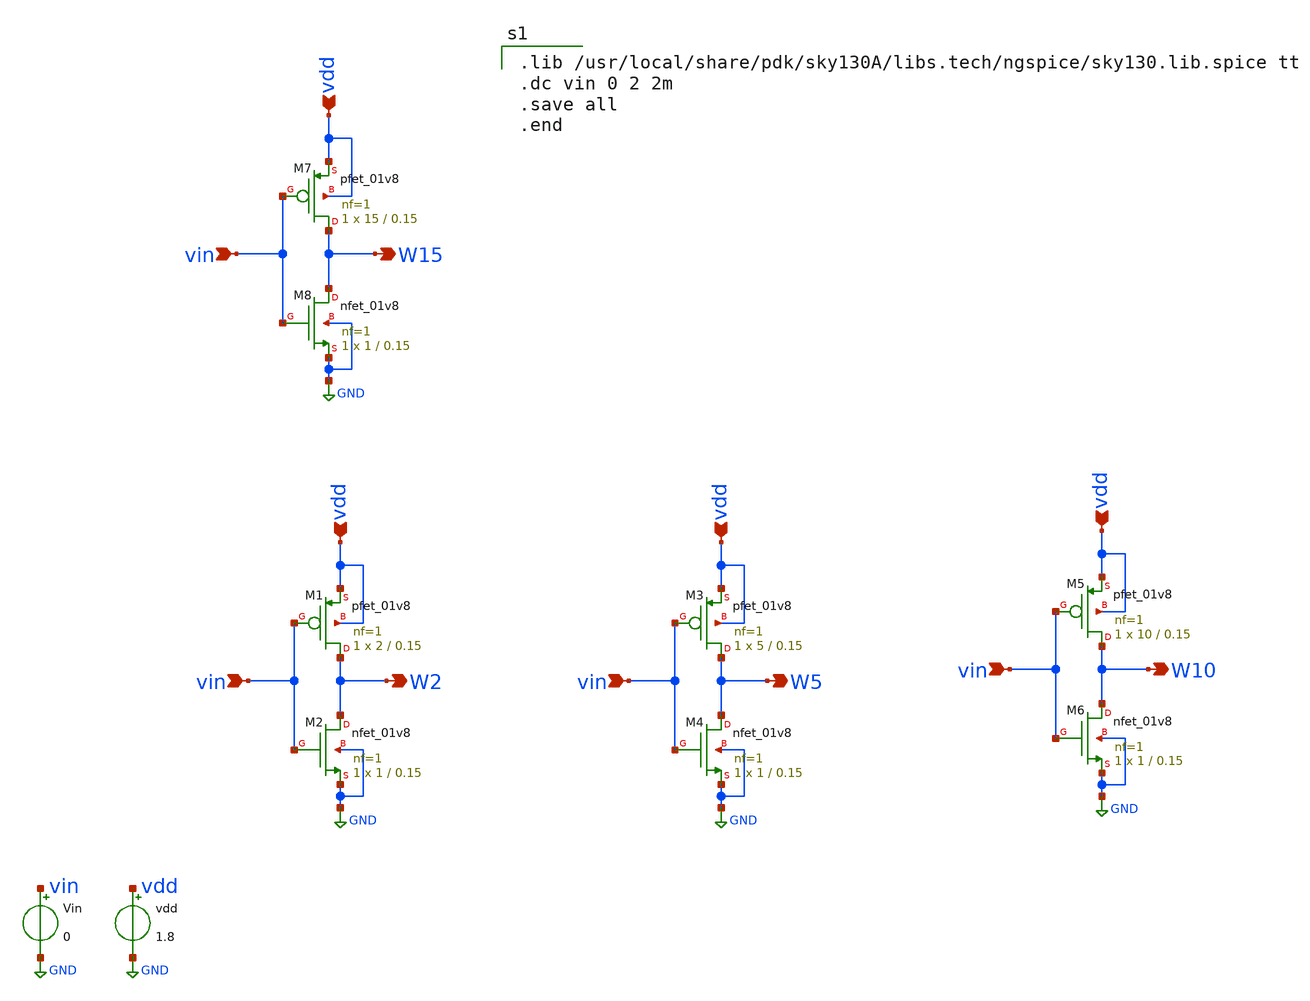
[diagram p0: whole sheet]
** sch_path: Inverter_vtc_testbench_sky130pdk.sch
**.subckt Inverter_vtc_testbench_sky130pdk vin vdd W2 vin vdd W5 vin vdd W10 vin vdd W15
*.ipin vin
*.ipin vdd
*.opin W2
*.ipin vin
*.ipin vdd
*.opin W5
*.ipin vin
*.ipin vdd
*.opin W10
*.ipin vin
*.ipin vdd
*.opin W15
XM1 W2 vin vdd vdd sky130_fd_pr__pfet_01v8 L=0.15 W=2 nf=1 ad='int((nf+1)/2) * W/nf * 0.29' as='int((nf+2)/2) * W/nf * 0.29'
+ pd='2*int((nf+1)/2) * (W/nf + 0.29)' ps='2*int((nf+2)/2) * (W/nf + 0.29)' nrd='0.29 / W' nrs='0.29 / W'
+ sa=0 sb=0 sd=0 mult=1 m=1
XM2 W2 vin GND GND sky130_fd_pr__nfet_01v8 L=0.15 W=1 nf=1 ad='int((nf+1)/2) * W/nf * 0.29' as='int((nf+2)/2) * W/nf * 0.29'
+ pd='2*int((nf+1)/2) * (W/nf + 0.29)' ps='2*int((nf+2)/2) * (W/nf + 0.29)' nrd='0.29 / W' nrs='0.29 / W'
+ sa=0 sb=0 sd=0 mult=1 m=1
XM3 W5 vin vdd vdd sky130_fd_pr__pfet_01v8 L=0.15 W=5 nf=1 ad='int((nf+1)/2) * W/nf * 0.29' as='int((nf+2)/2) * W/nf * 0.29'
+ pd='2*int((nf+1)/2) * (W/nf + 0.29)' ps='2*int((nf+2)/2) * (W/nf + 0.29)' nrd='0.29 / W' nrs='0.29 / W'
+ sa=0 sb=0 sd=0 mult=1 m=1
XM4 W5 vin GND GND sky130_fd_pr__nfet_01v8 L=0.15 W=1 nf=1 ad='int((nf+1)/2) * W/nf * 0.29' as='int((nf+2)/2) * W/nf * 0.29'
+ pd='2*int((nf+1)/2) * (W/nf + 0.29)' ps='2*int((nf+2)/2) * (W/nf + 0.29)' nrd='0.29 / W' nrs='0.29 / W'
+ sa=0 sb=0 sd=0 mult=1 m=1
XM5 W10 vin vdd vdd sky130_fd_pr__pfet_01v8 L=0.15 W=10 nf=1 ad='int((nf+1)/2) * W/nf * 0.29' as='int((nf+2)/2) * W/nf * 0.29'
+ pd='2*int((nf+1)/2) * (W/nf + 0.29)' ps='2*int((nf+2)/2) * (W/nf + 0.29)' nrd='0.29 / W' nrs='0.29 / W'
+ sa=0 sb=0 sd=0 mult=1 m=1
XM6 W10 vin GND GND sky130_fd_pr__nfet_01v8 L=0.15 W=1 nf=1 ad='int((nf+1)/2) * W/nf * 0.29' as='int((nf+2)/2) * W/nf * 0.29'
+ pd='2*int((nf+1)/2) * (W/nf + 0.29)' ps='2*int((nf+2)/2) * (W/nf + 0.29)' nrd='0.29 / W' nrs='0.29 / W'
+ sa=0 sb=0 sd=0 mult=1 m=1
Vin vin GND 0
vdd vdd GND 1.8
XM7 W15 vin vdd vdd sky130_fd_pr__pfet_01v8 L=0.15 W=15 nf=1 ad='int((nf+1)/2) * W/nf * 0.29' as='int((nf+2)/2) * W/nf * 0.29'
+ pd='2*int((nf+1)/2) * (W/nf + 0.29)' ps='2*int((nf+2)/2) * (W/nf + 0.29)' nrd='0.29 / W' nrs='0.29 / W'
+ sa=0 sb=0 sd=0 mult=1 m=1
XM8 W15 vin GND GND sky130_fd_pr__nfet_01v8 L=0.15 W=1 nf=1 ad='int((nf+1)/2) * W/nf * 0.29' as='int((nf+2)/2) * W/nf * 0.29'
+ pd='2*int((nf+1)/2) * (W/nf + 0.29)' ps='2*int((nf+2)/2) * (W/nf + 0.29)' nrd='0.29 / W' nrs='0.29 / W'
+ sa=0 sb=0 sd=0 mult=1 m=1
**** begin user architecture code

.lib /usr/local/share/pdk/sky130A/libs.tech/ngspice/sky130.lib.spice tt
.dc vin 0 2 2m
.save all
.end

**** end user architecture code
**.ends
.GLOBAL GND
.end
